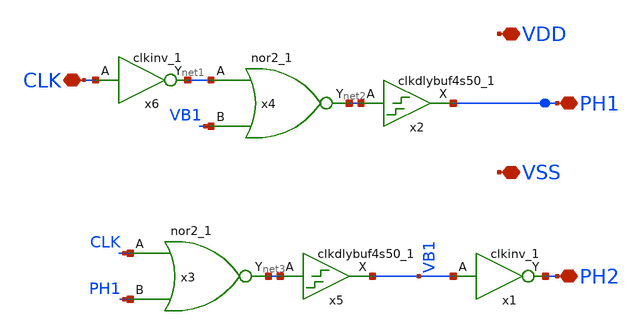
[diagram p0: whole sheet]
** sch_path: xschem/DC_DC_Converter_xschem/OTHERS/DC_DC_Converter_V7/Non_Overlap_Clk/Non_over_clk_V2.sch
**.subckt Non_over_clk_V2 VDD VSS CLK PH1 PH2
*.iopin VDD
*.iopin VSS
*.iopin CLK
*.iopin PH1
*.iopin PH2
x3 CLK PH1 VSS VSS VDD VDD net3 sky130_fd_sc_hd__nor2_1
x4 net1 VB1 VSS VSS VDD VDD net2 sky130_fd_sc_hd__nor2_1
x6 CLK VSS VSS VDD VDD net1 sky130_fd_sc_hd__clkinv_1
x2 net2 VSS VSS VDD VDD PH1 sky130_fd_sc_hd__clkdlybuf4s50_1
x5 net3 VSS VSS VDD VDD VB1 sky130_fd_sc_hd__clkdlybuf4s50_1
x1 VB1 VSS VSS VDD VDD PH2 sky130_fd_sc_hd__clkinv_1
**.ends
.end
